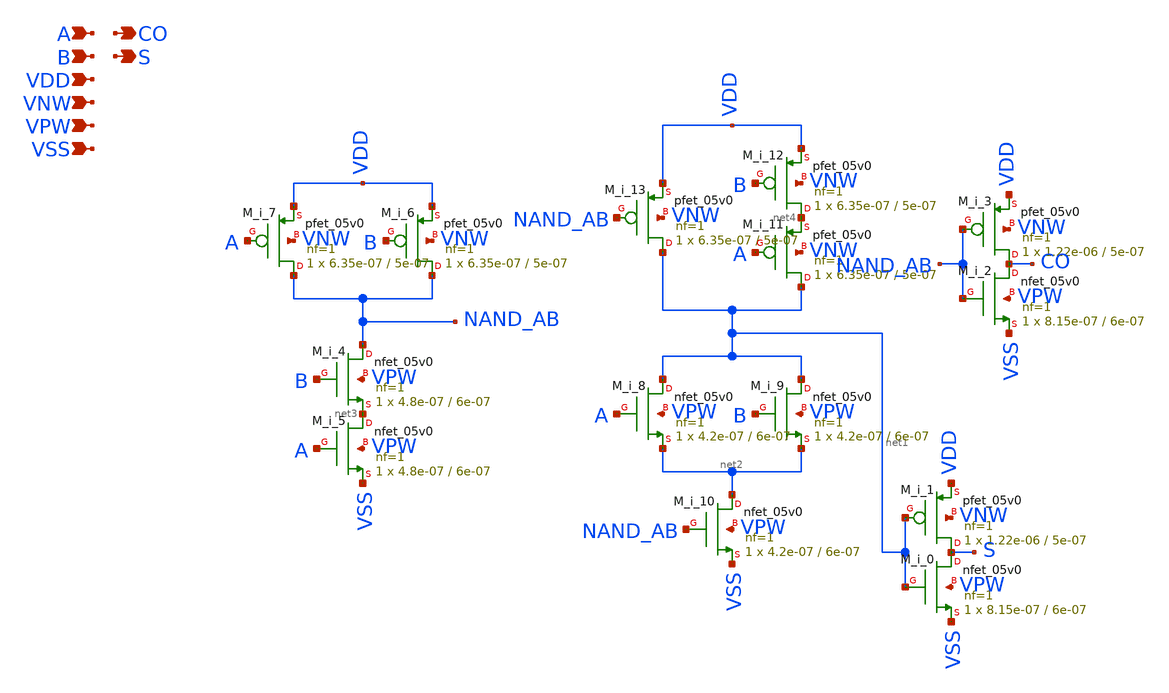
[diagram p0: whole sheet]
** sch_path: schematics/addh/gf180mcu_fd_sc_mcu7t5v0__addh_1.sch
**.subckt gf180mcu_fd_sc_mcu7t5v0__addh_1 A B CO S VDD VNW VPW VSS
*.ipin A
*.ipin B
*.opin CO
*.opin S
*.ipin VDD
*.ipin VNW
*.ipin VPW
*.ipin VSS
M_i_3 CO NAND_AB VDD VNW pfet_05v0 L=5e-07 W=1.22e-06 nf=1 ad='int((nf+1)/2) * W/nf * 0.18u' as='int((nf+2)/2) * W/nf * 0.18u'
+ pd='2*int((nf+1)/2) * (W/nf + 0.18u)' ps='2*int((nf+2)/2) * (W/nf + 0.18u)' nrd='0.18u / W' nrs='0.18u / W'
+ sa=0 sb=0 sd=0 m=1
M_i_2 CO NAND_AB VSS VPW nfet_05v0 L=6e-07 W=8.15e-07 nf=1 ad='int((nf+1)/2) * W/nf * 0.18u' as='int((nf+2)/2) * W/nf * 0.18u'
+ pd='2*int((nf+1)/2) * (W/nf + 0.18u)' ps='2*int((nf+2)/2) * (W/nf + 0.18u)' nrd='0.18u / W' nrs='0.18u / W'
+ sa=0 sb=0 sd=0 m=1
M_i_7 NAND_AB A VDD VNW pfet_05v0 L=5e-07 W=6.35e-07 nf=1 ad='int((nf+1)/2) * W/nf * 0.18u' as='int((nf+2)/2) * W/nf * 0.18u'
+ pd='2*int((nf+1)/2) * (W/nf + 0.18u)' ps='2*int((nf+2)/2) * (W/nf + 0.18u)' nrd='0.18u / W' nrs='0.18u / W'
+ sa=0 sb=0 sd=0 m=1
M_i_6 NAND_AB B VDD VNW pfet_05v0 L=5e-07 W=6.35e-07 nf=1 ad='int((nf+1)/2) * W/nf * 0.18u' as='int((nf+2)/2) * W/nf * 0.18u'
+ pd='2*int((nf+1)/2) * (W/nf + 0.18u)' ps='2*int((nf+2)/2) * (W/nf + 0.18u)' nrd='0.18u / W' nrs='0.18u / W'
+ sa=0 sb=0 sd=0 m=1
M_i_4 NAND_AB B net3 VPW nfet_05v0 L=6e-07 W=4.8e-07 nf=1 ad='int((nf+1)/2) * W/nf * 0.18u' as='int((nf+2)/2) * W/nf * 0.18u'
+ pd='2*int((nf+1)/2) * (W/nf + 0.18u)' ps='2*int((nf+2)/2) * (W/nf + 0.18u)' nrd='0.18u / W' nrs='0.18u / W'
+ sa=0 sb=0 sd=0 m=1
M_i_5 net3 A VSS VPW nfet_05v0 L=6e-07 W=4.8e-07 nf=1 ad='int((nf+1)/2) * W/nf * 0.18u' as='int((nf+2)/2) * W/nf * 0.18u'
+ pd='2*int((nf+1)/2) * (W/nf + 0.18u)' ps='2*int((nf+2)/2) * (W/nf + 0.18u)' nrd='0.18u / W' nrs='0.18u / W'
+ sa=0 sb=0 sd=0 m=1
M_i_13 net1 NAND_AB VDD VNW pfet_05v0 L=5e-07 W=6.35e-07 nf=1 ad='int((nf+1)/2) * W/nf * 0.18u' as='int((nf+2)/2) * W/nf * 0.18u'
+ pd='2*int((nf+1)/2) * (W/nf + 0.18u)' ps='2*int((nf+2)/2) * (W/nf + 0.18u)' nrd='0.18u / W' nrs='0.18u / W'
+ sa=0 sb=0 sd=0 m=1
M_i_12 net4 B VDD VNW pfet_05v0 L=5e-07 W=6.35e-07 nf=1 ad='int((nf+1)/2) * W/nf * 0.18u' as='int((nf+2)/2) * W/nf * 0.18u'
+ pd='2*int((nf+1)/2) * (W/nf + 0.18u)' ps='2*int((nf+2)/2) * (W/nf + 0.18u)' nrd='0.18u / W' nrs='0.18u / W'
+ sa=0 sb=0 sd=0 m=1
M_i_11 net1 A net4 VNW pfet_05v0 L=5e-07 W=6.35e-07 nf=1 ad='int((nf+1)/2) * W/nf * 0.18u' as='int((nf+2)/2) * W/nf * 0.18u'
+ pd='2*int((nf+1)/2) * (W/nf + 0.18u)' ps='2*int((nf+2)/2) * (W/nf + 0.18u)' nrd='0.18u / W' nrs='0.18u / W'
+ sa=0 sb=0 sd=0 m=1
M_i_8 net1 A net2 VPW nfet_05v0 L=6e-07 W=4.2e-07 nf=1 ad='int((nf+1)/2) * W/nf * 0.18u' as='int((nf+2)/2) * W/nf * 0.18u'
+ pd='2*int((nf+1)/2) * (W/nf + 0.18u)' ps='2*int((nf+2)/2) * (W/nf + 0.18u)' nrd='0.18u / W' nrs='0.18u / W'
+ sa=0 sb=0 sd=0 m=1
M_i_9 net1 B net2 VPW nfet_05v0 L=6e-07 W=4.2e-07 nf=1 ad='int((nf+1)/2) * W/nf * 0.18u' as='int((nf+2)/2) * W/nf * 0.18u'
+ pd='2*int((nf+1)/2) * (W/nf + 0.18u)' ps='2*int((nf+2)/2) * (W/nf + 0.18u)' nrd='0.18u / W' nrs='0.18u / W'
+ sa=0 sb=0 sd=0 m=1
M_i_10 net2 NAND_AB VSS VPW nfet_05v0 L=6e-07 W=4.2e-07 nf=1 ad='int((nf+1)/2) * W/nf * 0.18u' as='int((nf+2)/2) * W/nf * 0.18u'
+ pd='2*int((nf+1)/2) * (W/nf + 0.18u)' ps='2*int((nf+2)/2) * (W/nf + 0.18u)' nrd='0.18u / W' nrs='0.18u / W'
+ sa=0 sb=0 sd=0 m=1
M_i_1 S net1 VDD VNW pfet_05v0 L=5e-07 W=1.22e-06 nf=1 ad='int((nf+1)/2) * W/nf * 0.18u' as='int((nf+2)/2) * W/nf * 0.18u'
+ pd='2*int((nf+1)/2) * (W/nf + 0.18u)' ps='2*int((nf+2)/2) * (W/nf + 0.18u)' nrd='0.18u / W' nrs='0.18u / W'
+ sa=0 sb=0 sd=0 m=1
M_i_0 S net1 VSS VPW nfet_05v0 L=6e-07 W=8.15e-07 nf=1 ad='int((nf+1)/2) * W/nf * 0.18u' as='int((nf+2)/2) * W/nf * 0.18u'
+ pd='2*int((nf+1)/2) * (W/nf + 0.18u)' ps='2*int((nf+2)/2) * (W/nf + 0.18u)' nrd='0.18u / W' nrs='0.18u / W'
+ sa=0 sb=0 sd=0 m=1
**.ends
.end
